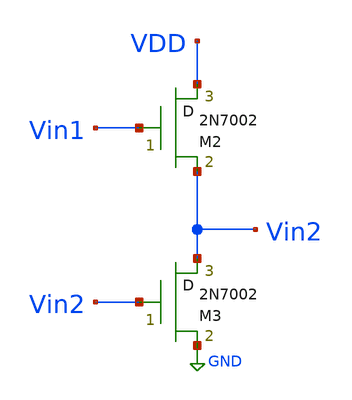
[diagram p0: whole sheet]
** sch_path: ISSCC25/submitted_notebooks/MicroNina/sch/SourceFollower.sch
**.subckt SourceFollower
M2 VDD Vin1 Vin2 M2N7002 m=1
M3 Vin2 Vin2 GND M2N7002 m=1
**.ends
.GLOBAL GND
.end
